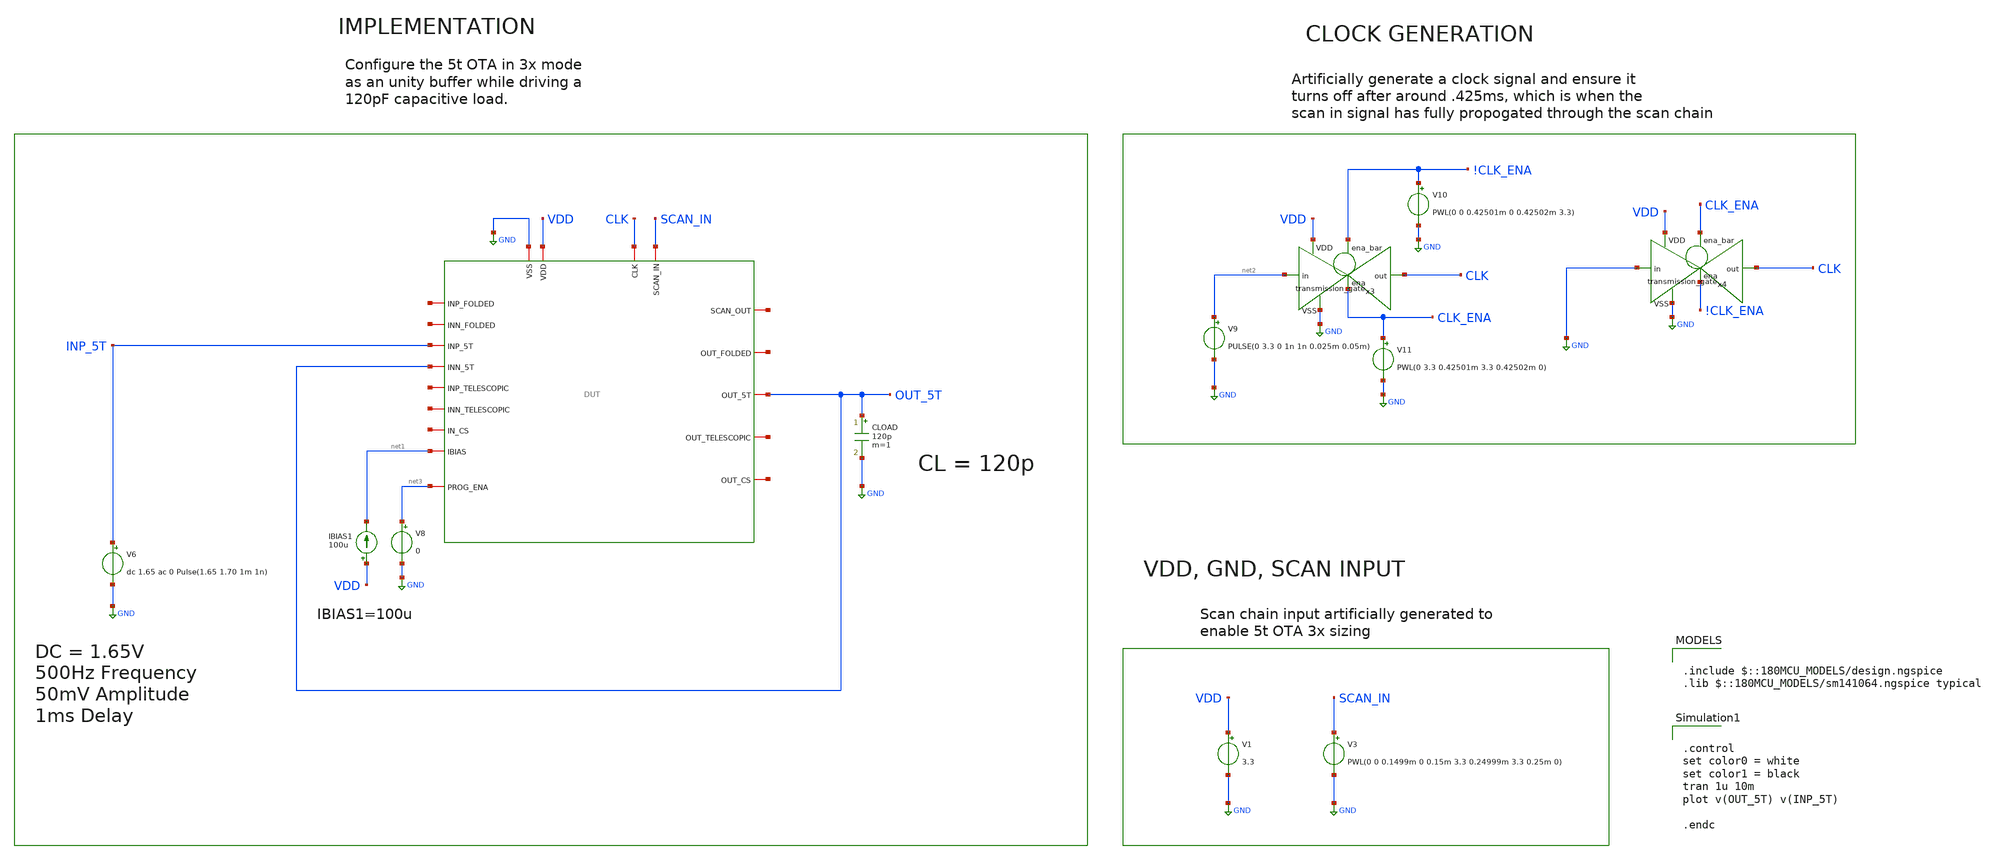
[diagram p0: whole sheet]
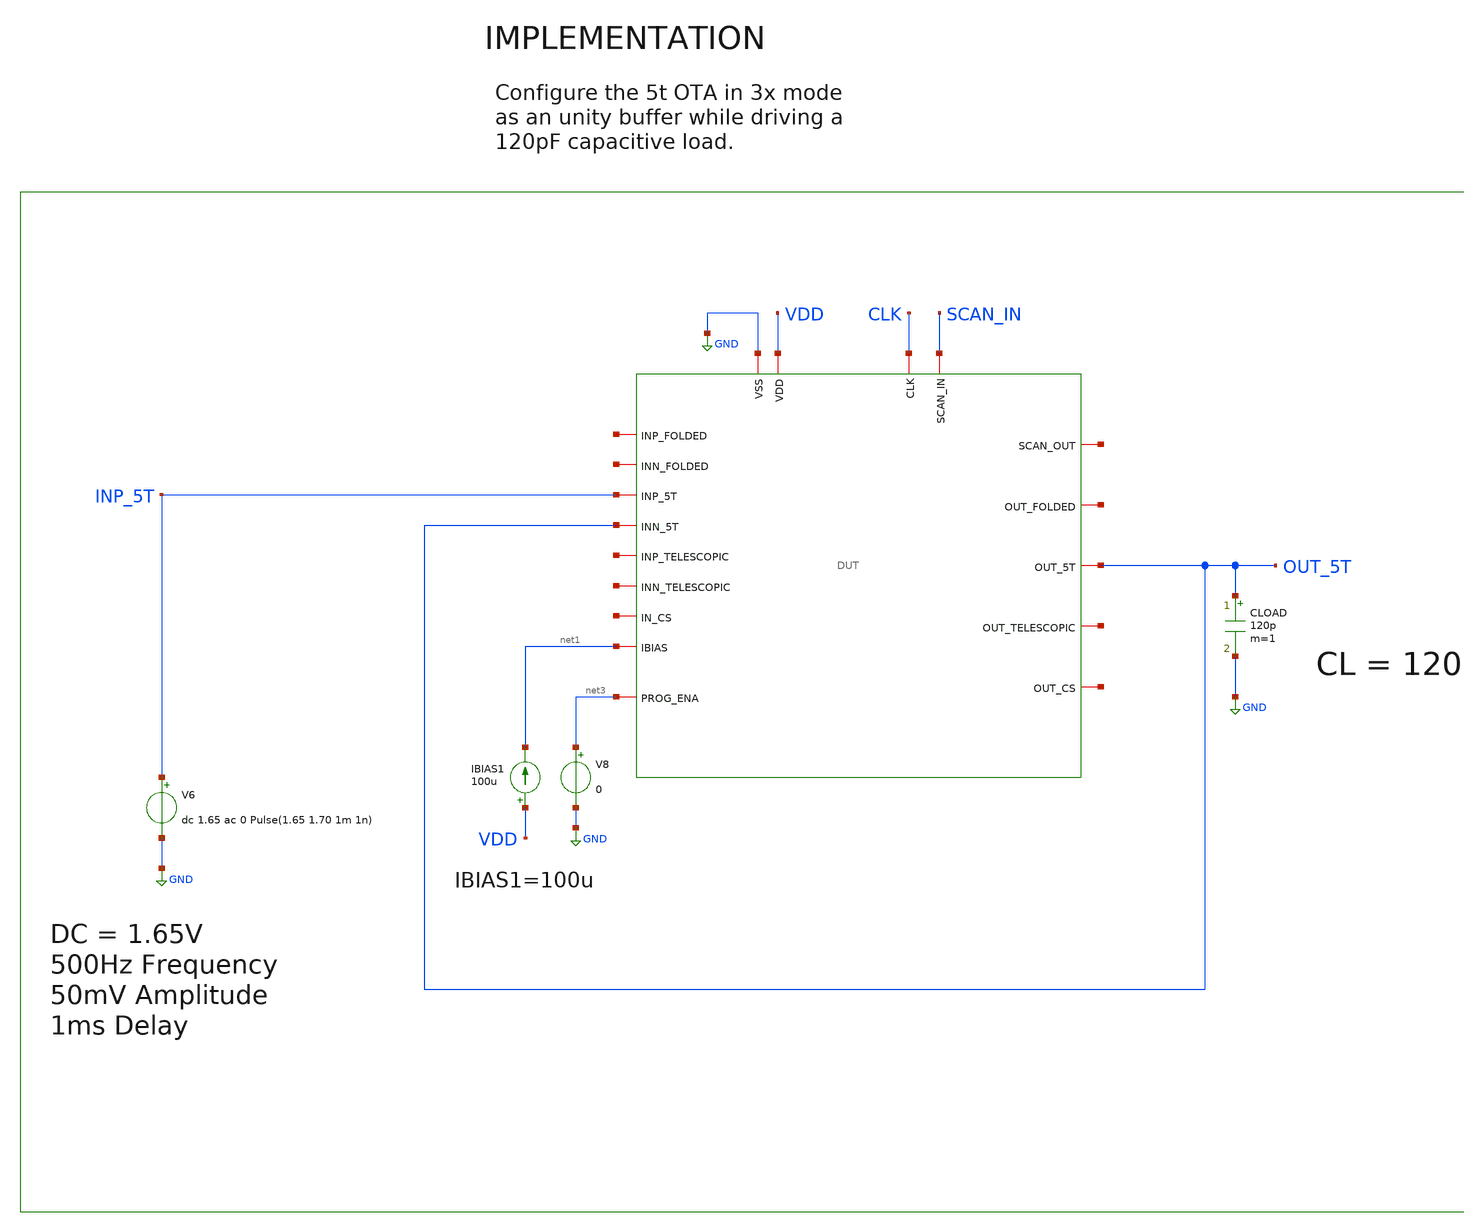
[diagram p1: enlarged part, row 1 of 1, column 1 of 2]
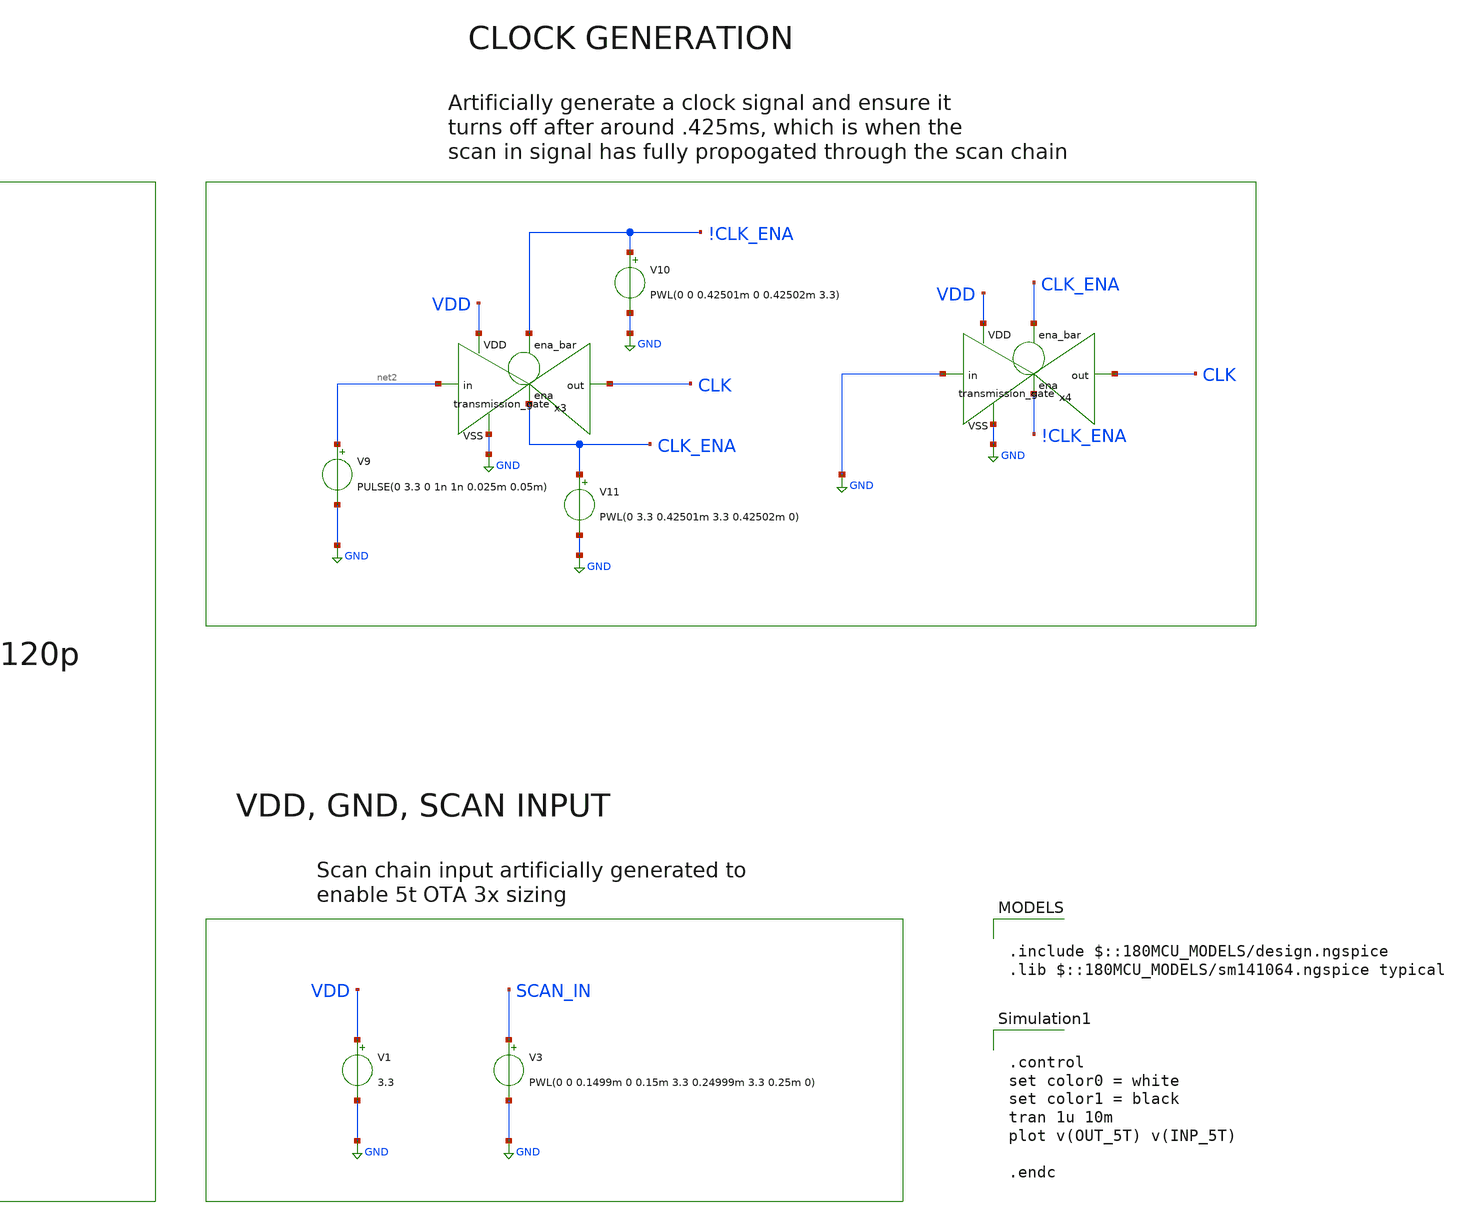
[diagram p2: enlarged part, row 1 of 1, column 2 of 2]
** sch_path: designs/libs/core_tb/sl/ota_5t/5t_unity_step_3x.sch
**.subckt 5t_unity_step_3x
V3 SCAN_IN GND PWL(0 0 0.1499m 0 0.15m 3.3 0.24999m 3.3 0.25m 0)
V1 VDD GND 3.3
IBIAS1 VDD net1 100u
CLOAD OUT_5T GND 120p m=1
V6 INP_5T GND dc 1.65 ac 0 Pulse(1.65 1.70 1m 1n)
x1 CLK net4 SCAN_IN GND VDD net5 net6 OUT_5T net1 net7 INP_5T OUT_5T net8 net9 net10 net11 net12
+ net3 DUT
V9 net2 GND PULSE(0 3.3 0 1n 1n 0.025m 0.05m)
x3 !CLK_ENA VDD CLK net2 GND CLK_ENA transmission_gate
V10 !CLK_ENA GND PWL(0 0 0.42501m 0 0.42502m 3.3)
V11 CLK_ENA GND PWL(0 3.3 0.42501m 3.3 0.42502m 0)
x4 CLK_ENA VDD CLK GND GND !CLK_ENA transmission_gate
V8 net3 GND 0
**** begin user architecture code

.include $::180MCU_MODELS/design.ngspice
.lib $::180MCU_MODELS/sm141064.ngspice typical



.control
set color0 = white
set color1 = black
tran 1u 10m
plot v(OUT_5T) v(INP_5T)

.endc


**** end user architecture code
**.ends
.GLOBAL GND
.end
